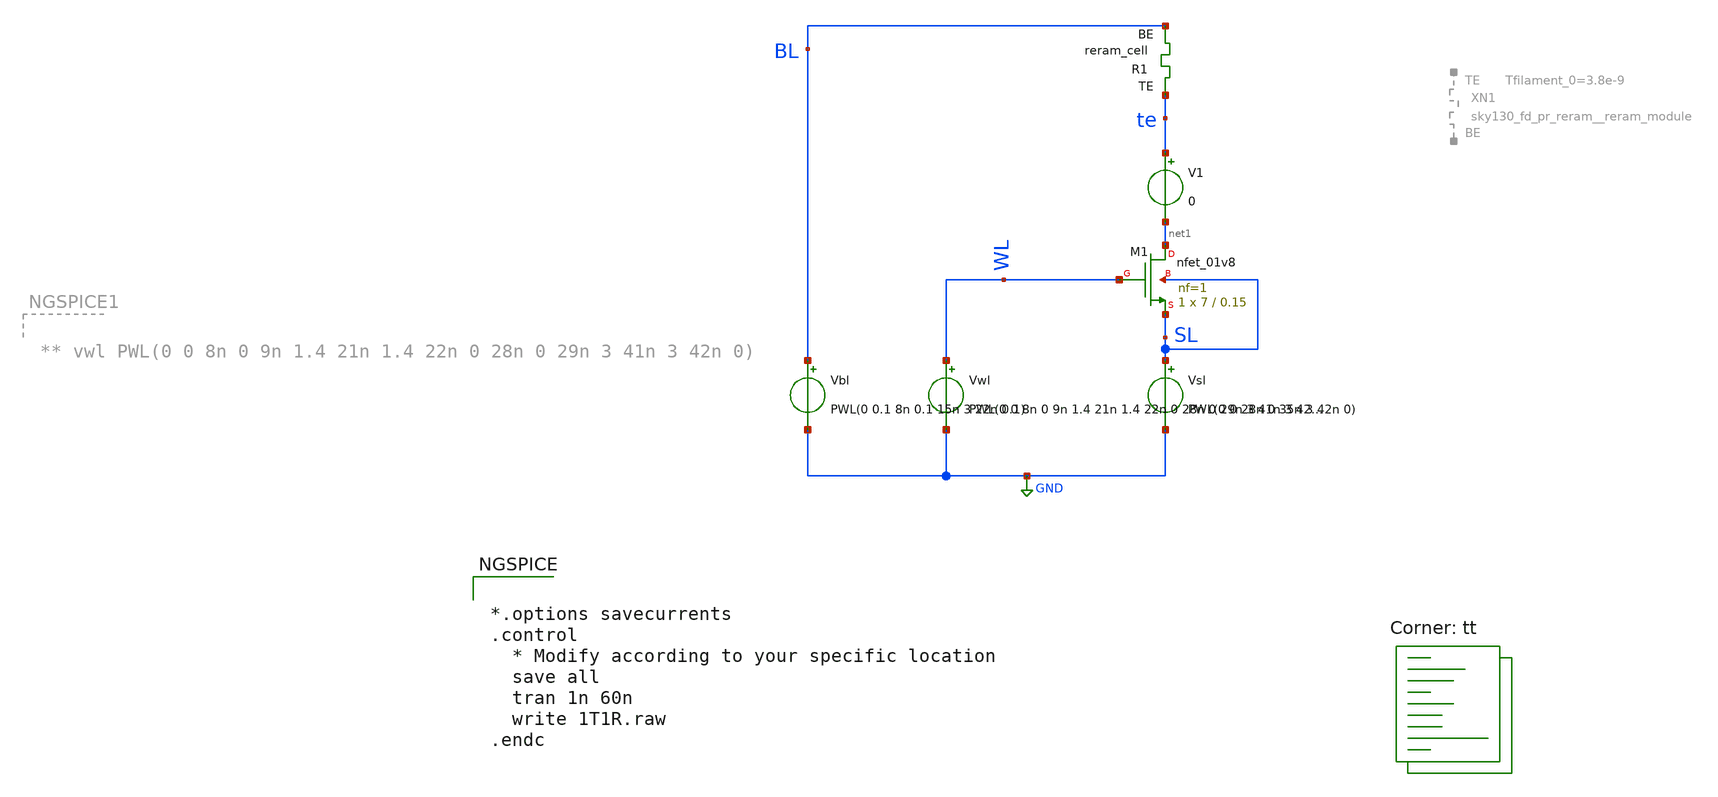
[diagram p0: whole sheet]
** sch_path: memristor_models/sky130_original/1T1R.sch
**.subckt 1T1R
XM1 net1 WL SL SL sky130_fd_pr__nfet_01v8 L=0.15 W=7 nf=1 ad='int((nf+1)/2) * W/nf * 0.29' as='int((nf+2)/2) * W/nf * 0.29'
+ pd='2*int((nf+1)/2) * (W/nf + 0.29)' ps='2*int((nf+2)/2) * (W/nf + 0.29)' nrd='0.29 / W' nrs='0.29 / W'
+ sa=0 sb=0 sd=0 mult=1 m=1
Vwl WL GND PWL(0 0 8n 0 9n 1.4 21n 1.4 22n 0 28n 0 29n 3 41n 3 42n 0)
Vbl BL GND PWL(0 0.1 8n 0.1 15n 3 22n 0.1)
V1 te net1 0
XR1 te BL sky130_fd_pr_reram__reram_cell Tfilament_0=3e-9
Vsl SL GND PWL(0 0 28n 0 35n 3 42n 0)
**** begin user architecture code


*.options savecurrents
.control
  * Modify according to your specific location
  save all
  tran 1n 60n
  write 1T1R.raw
.endc



.lib $::SKYWATER_MODELS/sky130.lib.spice tt

** opencircuitdesign pdks install
.inc $::SKYWATER_MODELS/sky130_fd_pr_reram__reram_cell.spice

**** end user architecture code
**.ends
.GLOBAL GND
.end
